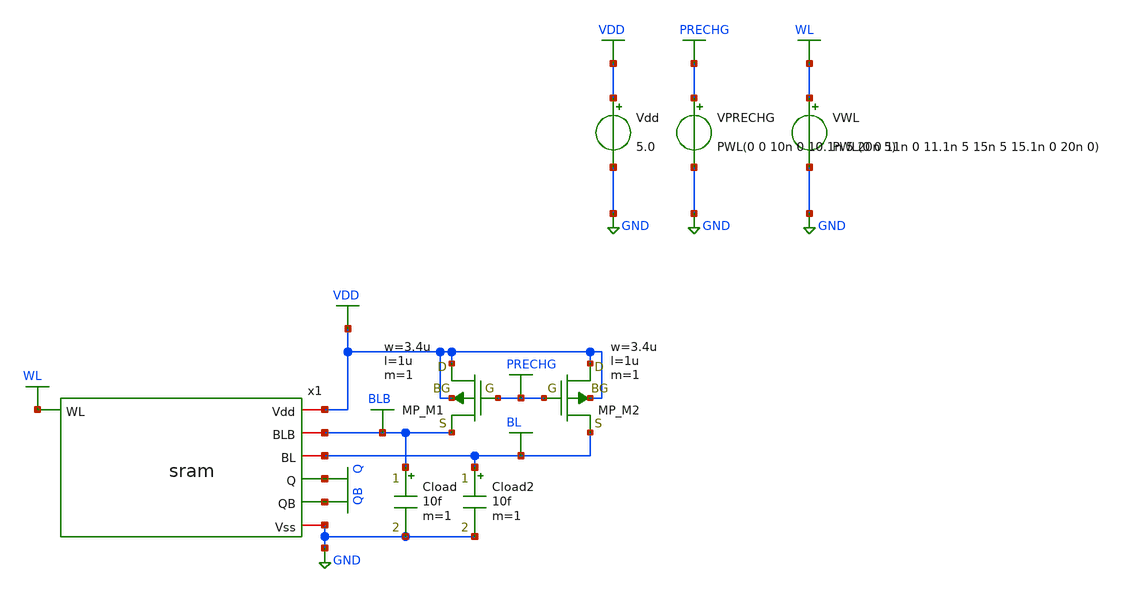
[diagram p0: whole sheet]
** sch_path: sram_tb_tran_read.sch
**.subckt sram_tb_tran_read
Vdd VDD GND 5.0
VWL WL GND PWL(0 0 11n 0 11.1n 5 15n 5 15.1n 0 20n 0)
x1 WL VDD BLB BL Q QB GND sram
XM1 VDD PRECHG BLB VDD PMOS w=3.4u l=1u as=0 ad=0 ps=0 pd=0 nrd=0 nrs=0 m=1
XM2 VDD PRECHG BL VDD PMOS w=3.4u l=1u as=0 ad=0 ps=0 pd=0 nrd=0 nrs=0 m=1
Cload BLB GND 10f m=1
Cload2 BL GND 10f m=1
VPRECHG PRECHG GND PWL(0 0 10n 0 10.1n 5 20n 5)
**** begin user architecture code
 .include $::LIB/ip62_models


.param QINIT=0 QBINIT=5
.ic v(Q)='QINIT' v(QB)='QBINIT'

.control
save all @m.x1.xxm7.m1[id] @m.x1.xxm6.m1[id]

tran 0.01n 20n

meas tran BL_read_Q0 find v(BL) at=14n
meas tran BLB_read_Q0 find v(BLB) at=14n
meas tran Q_read_Q0 find v(Q) at=14n
meas tran QB_read_Q0 find v(QB) at=14n
meas tran Q_disturb_Q0 max v(Q) from=11n to=15n
meas tran Q_hold_Q0 find v(Q) at=18n
meas tran QB_hold_Q0 find v(QB) at=18n

let PRECHG_T = V(PRECHG)/5+10
let WL_T = V(WL)/5+8
let BL_T = V(BL)/5+6
let BLB_T = V(BLB)/5+4
let Q_T = V(Q)/5+2
let QB_T = V(QB)/5
let I_Q_ACCESS_uA = @m.x1.xxm7.m1[id]*1e6
let I_QB_ACCESS_uA = @m.x1.xxm6.m1[id]*1e6
let I_Q_ACCESS_MAG_uA = abs(I_Q_ACCESS_uA)
let I_QB_ACCESS_MAG_uA = abs(I_QB_ACCESS_uA)
meas tran I_Q_ACCESS_PEAK_Q0 max I_Q_ACCESS_MAG_uA from=11n to=15n
meas tran I_QB_ACCESS_PEAK_Q0 max I_QB_ACCESS_MAG_uA from=11n to=15n
plot PRECHG_T WL_T BL_T BLB_T Q_T QB_T ylimit -0.2 11.2 ydelta 1 title 'READ: Q=0, QB=5 V'
plot I_Q_ACCESS_uA I_QB_ACCESS_uA ylabel 'Access current (uA)' title 'READ current: Q=0, QB=5 V'

alterparam QINIT=5
alterparam QBINIT=0
reset
save all @m.x1.xxm7.m1[id] @m.x1.xxm6.m1[id]

tran 0.01n 20n

meas tran BL_read_Q5 find v(BL) at=14n
meas tran BLB_read_Q5 find v(BLB) at=14n
meas tran Q_read_Q5 find v(Q) at=14n
meas tran QB_read_Q5 find v(QB) at=14n
meas tran QB_disturb_Q5 max v(QB) from=11n to=15n
meas tran Q_hold_Q5 find v(Q) at=18n
meas tran QB_hold_Q5 find v(QB) at=18n

let PRECHG_T = V(PRECHG)/5+10
let WL_T = V(WL)/5+8
let BL_T = V(BL)/5+6
let BLB_T = V(BLB)/5+4
let Q_T = V(Q)/5+2
let QB_T = V(QB)/5
let I_Q_ACCESS_uA = @m.x1.xxm7.m1[id]*1e6
let I_QB_ACCESS_uA = @m.x1.xxm6.m1[id]*1e6
let I_Q_ACCESS_MAG_uA = abs(I_Q_ACCESS_uA)
let I_QB_ACCESS_MAG_uA = abs(I_QB_ACCESS_uA)
meas tran I_Q_ACCESS_PEAK_Q5 max I_Q_ACCESS_MAG_uA from=11n to=15n
meas tran I_QB_ACCESS_PEAK_Q5 max I_QB_ACCESS_MAG_uA from=11n to=15n
plot PRECHG_T WL_T BL_T BLB_T Q_T QB_T ylimit -0.2 11.2 ydelta 1 title 'READ: Q=5 V, QB=0'
plot I_Q_ACCESS_uA I_QB_ACCESS_uA ylabel 'Access current (uA)' title 'READ current: Q=5 V, QB=0'

.endc



**** end user architecture code
**.ends

* expanding   symbol:  sram.sym # of pins=7
** sym_path: sram.sym
** sch_path: sram.sch
.subckt sram WL Vdd BLB BL Q QB Vss
*.iopin Vdd
*.iopin Vss
*.iopin BLB
*.iopin BL
*.ipin WL
*.opin Q
*.opin QB
XXM1 Q QB Vss Vss NMOS w=3.4u l=1u nrd=0 nrs=0 m=1
XXM2 Q QB Vdd Vdd PMOS w=3.4u l=1u nrd=0 nrs=0 m=1
XXM3 QB Q Vss Vss NMOS w=3.4u l=1u nrd=0 nrs=0 m=1
XXM4 QB Q Vdd Vdd PMOS w=3.4u l=1u nrd=0 nrs=0 m=1
XXM7 Q WL BL Vss NMOS w=3.4u l=1u nrd=0 nrs=0 m=1
XXM6 QB WL BLB Vss NMOS w=3.4u l=1u nrd=0 nrs=0 m=1
.ends

.GLOBAL VDD
.GLOBAL GND
.GLOBAL QB
.GLOBAL Q
.GLOBAL BLB
.GLOBAL WL
.GLOBAL BL
.GLOBAL PRECHG
.end
